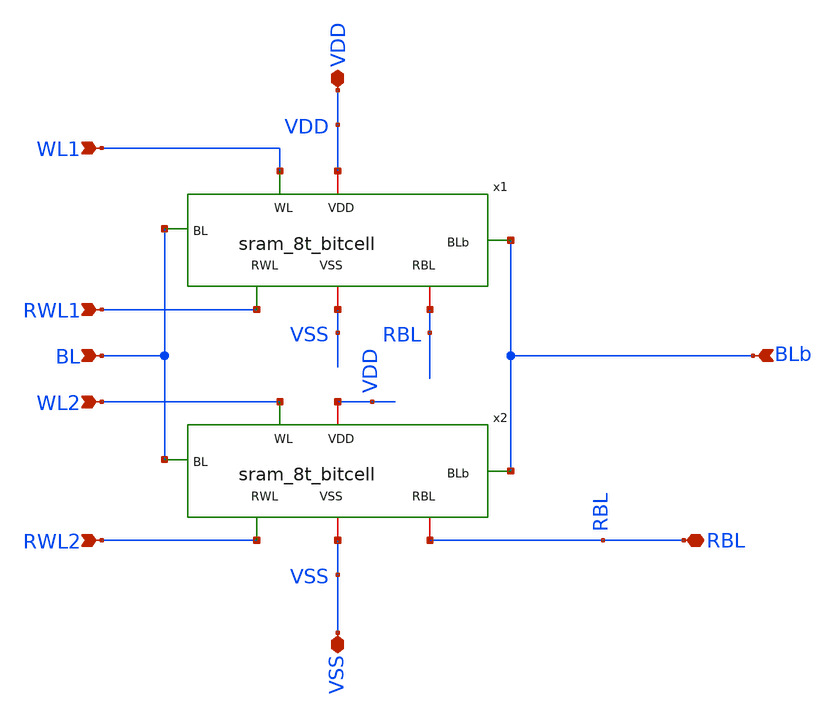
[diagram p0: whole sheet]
** sch_path: schematics/row_2cell.sch
**.subckt row_2cell WL1 WL2 RWL1 RWL2 BL VDD VSS BLb RBL
*.ipin WL1
*.ipin WL2
*.ipin RWL1
*.ipin RWL2
*.ipin BL
*.iopin VDD
*.iopin VSS
*.ipin BLb
*.iopin RBL
x1 VDD WL1 BL BLb RWL1 VSS RBL sram_8t_bitcell
x2 VDD WL2 BL BLb RWL2 VSS RBL sram_8t_bitcell
**.ends
.end
